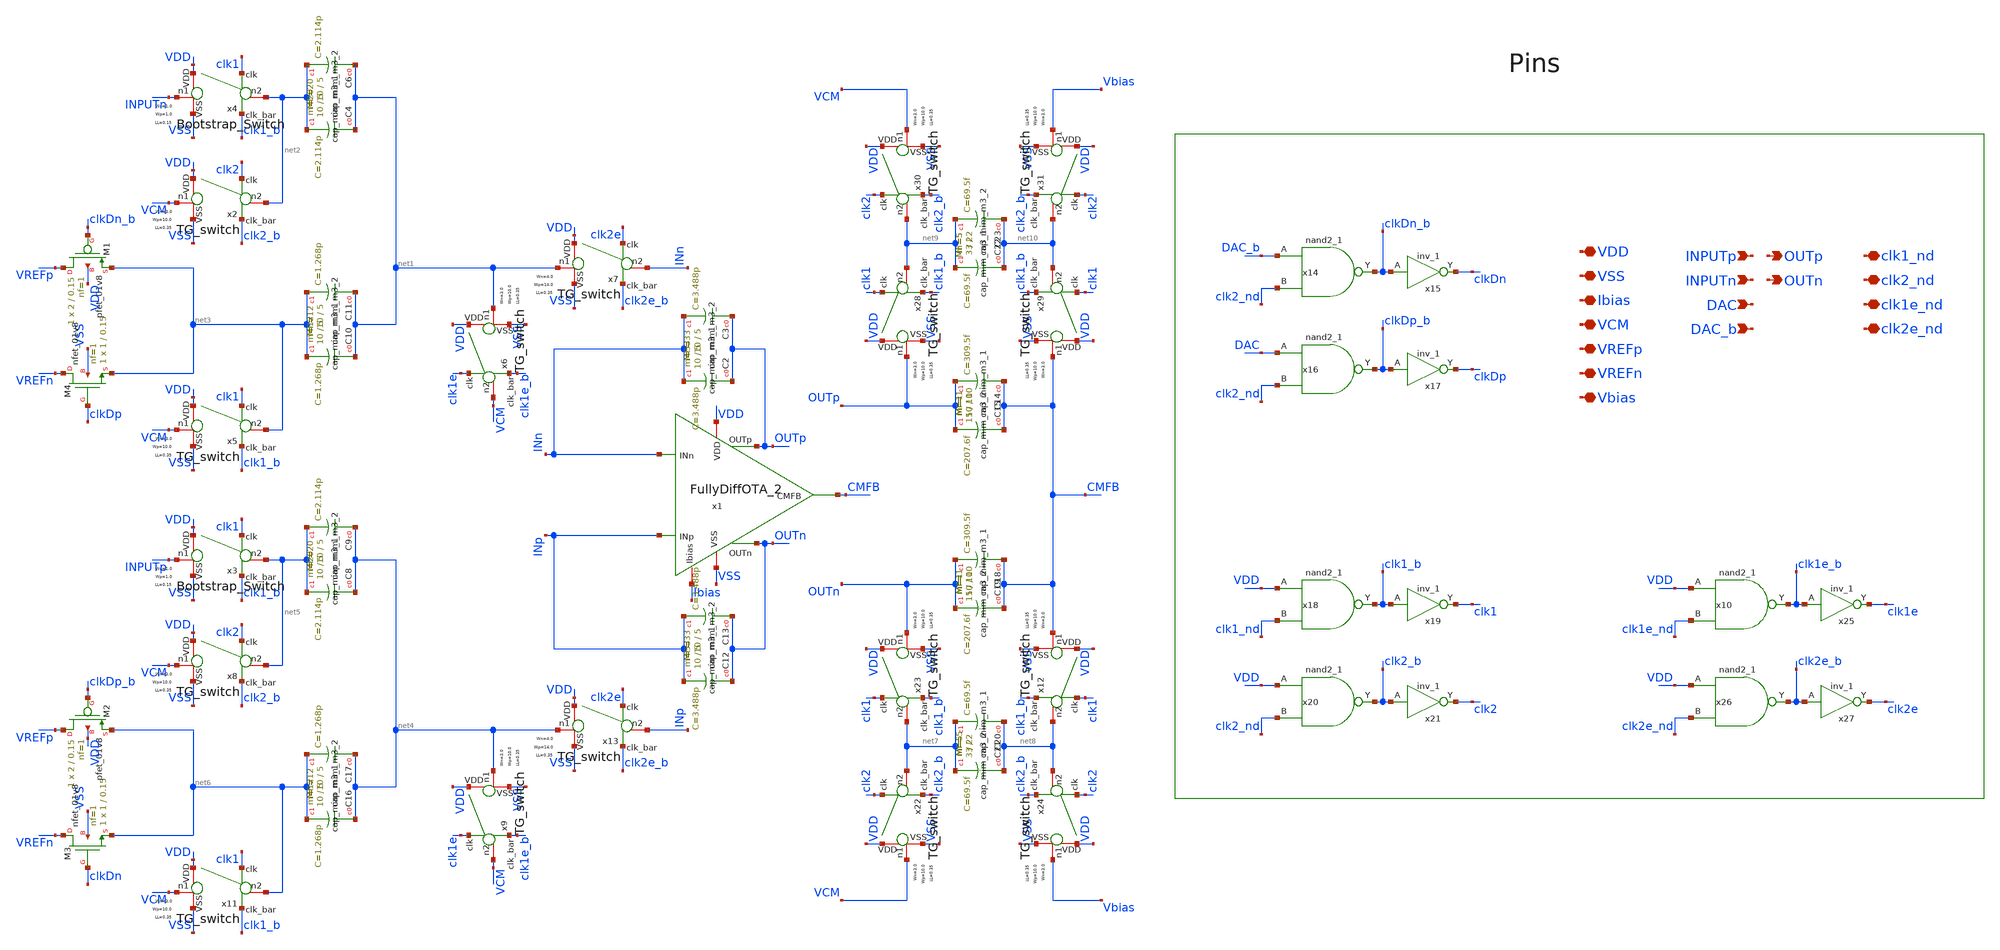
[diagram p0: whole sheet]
** sch_path: xschem/lib/Analog/SC_Integrator_2.sch
**.subckt SC_Integrator_2 clk2e_nd clk1e_nd clk2_nd clk1_nd VDD VSS VCM Ibias INPUTp INPUTn VREFp
*+ VREFn Vbias DAC DAC_b OUTp OUTn
*.iopin clk2e_nd
*.iopin clk1e_nd
*.iopin clk2_nd
*.iopin clk1_nd
*.iopin VDD
*.iopin VSS
*.iopin VCM
*.iopin Ibias
*.ipin INPUTp
*.ipin INPUTn
*.iopin VREFp
*.iopin VREFn
*.iopin Vbias
*.ipin DAC
*.ipin DAC_b
*.opin OUTp
*.opin OUTn
x14 DAC_b clk2_nd VSS VSS VDD VDD clkDn_b sky130_fd_sc_hd__nand2_1
x15 clkDn_b VSS VSS VDD VDD clkDn sky130_fd_sc_hd__inv_1
x16 DAC clk2_nd VSS VSS VDD VDD clkDp_b sky130_fd_sc_hd__nand2_1
x17 clkDp_b VSS VSS VDD VDD clkDp sky130_fd_sc_hd__inv_1
x18 VDD clk1_nd VSS VSS VDD VDD clk1_b sky130_fd_sc_hd__nand2_1
x19 clk1_b VSS VSS VDD VDD clk1 sky130_fd_sc_hd__inv_1
x20 VDD clk2_nd VSS VSS VDD VDD clk2_b sky130_fd_sc_hd__nand2_1
x21 clk2_b VSS VSS VDD VDD clk2 sky130_fd_sc_hd__inv_1
x10 VDD clk1e_nd VSS VSS VDD VDD clk1e_b sky130_fd_sc_hd__nand2_1
x25 clk1e_b VSS VSS VDD VDD clk1e sky130_fd_sc_hd__inv_1
x26 VDD clk2e_nd VSS VSS VDD VDD clk2e_b sky130_fd_sc_hd__nand2_1
x27 clk2e_b VSS VSS VDD VDD clk2e sky130_fd_sc_hd__inv_1
XM2 VREFp clkDp_b net6 VDD sky130_fd_pr__pfet_01v8 L=0.15 W=2 nf=1 ad='int((1 + 1)/2) * 2 / 1 * 0.29'
+ as='int((1 + 2)/2) * 2 / 1 * 0.29' pd='2*int((1 + 1)/2) * (2 / 1 + 0.29)' ps='2*int((1 + 2)/2) * (2 / 1 + 0.29)'
+ nrd='0.29 / 2 ' nrs='0.29 / 2 ' sa=0 sb=0 sd=0 mult=1 m=1
XM1 VREFp clkDn_b net3 VDD sky130_fd_pr__pfet_01v8 L=0.15 W=2 nf=1 ad='int((1 + 1)/2) * 2 / 1 * 0.29'
+ as='int((1 + 2)/2) * 2 / 1 * 0.29' pd='2*int((1 + 1)/2) * (2 / 1 + 0.29)' ps='2*int((1 + 2)/2) * (2 / 1 + 0.29)'
+ nrd='0.29 / 2 ' nrs='0.29 / 2 ' sa=0 sb=0 sd=0 mult=1 m=1
XM3 VREFn clkDn net6 VSS sky130_fd_pr__nfet_01v8 L=0.15 W=1 nf=1 ad='int((1 + 1)/2) * 1 / 1 * 0.29' as='int((1 + 2)/2) * 1 / 1 * 0.29'
+ pd='2*int((1 + 1)/2) * (1 / 1 + 0.29)' ps='2*int((1 + 2)/2) * (1 / 1 + 0.29)' nrd='0.29 / 1 ' nrs='0.29 / 1 '
+ sa=0 sb=0 sd=0 mult=1 m=1
XM4 VREFn clkDp net3 VSS sky130_fd_pr__nfet_01v8 L=0.15 W=1 nf=1 ad='int((1 + 1)/2) * 1 / 1 * 0.29' as='int((1 + 2)/2) * 1 / 1 * 0.29'
+ pd='2*int((1 + 1)/2) * (1 / 1 + 0.29)' ps='2*int((1 + 2)/2) * (1 / 1 + 0.29)' nrd='0.29 / 1 ' nrs='0.29 / 1 '
+ sa=0 sb=0 sd=0 mult=1 m=1
x4 clk1_b clk1 VDD VSS INPUTn net2 Bootstrap_Switch Wn=1.0 Wp=1.0 LL=0.15
x3 clk1_b clk1 VDD VSS INPUTp net5 Bootstrap_Switch Wn=1.0 Wp=1.0 LL=0.15
x6 clk1e_b clk1e VDD VSS net1 VCM TG_switch Wn=3.0 Wp=10.0 LL=0.35
x9 clk1e_b clk1e VDD VSS net4 VCM TG_switch Wn=3.0 Wp=10.0 LL=0.35
x2 clk2_b clk2 VDD VSS VCM net2 TG_switch Wn=3.0 Wp=10.0 LL=0.35
x5 clk1_b clk1 VDD VSS VCM net3 TG_switch Wn=3.0 Wp=10.0 LL=0.35
x8 clk2_b clk2 VDD VSS VCM net5 TG_switch Wn=3.0 Wp=10.0 LL=0.35
x11 clk1_b clk1 VDD VSS VCM net6 TG_switch Wn=3.0 Wp=10.0 LL=0.35
x7 clk2e_b clk2e VDD VSS net1 INn TG_switch Wn=4.0 Wp=14.0 LL=0.35
x13 clk2e_b clk2e VDD VSS net4 INp TG_switch Wn=4.0 Wp=14.0 LL=0.35
XC14 CMFB OUTp sky130_fd_pr__cap_mim_m3_2 W=15 L=10 MF=1 m=1
XC15 CMFB OUTp sky130_fd_pr__cap_mim_m3_1 W=10 L=10 MF=1 m=1
XC18 CMFB OUTn sky130_fd_pr__cap_mim_m3_2 W=15 L=10 MF=1 m=1
XC19 CMFB OUTn sky130_fd_pr__cap_mim_m3_1 W=10 L=10 MF=1 m=1
x23 clk1_b clk1 VDD VSS OUTn net7 TG_switch Wn=3.0 Wp=10.0 LL=0.35
x12 clk1_b clk1 VDD VSS CMFB net8 TG_switch Wn=3.0 Wp=10.0 LL=0.35
x22 clk2_b clk2 VDD VSS VCM net7 TG_switch Wn=3.0 Wp=10.0 LL=0.35
x24 clk2_b clk2 VDD VSS Vbias net8 TG_switch Wn=3.0 Wp=10.0 LL=0.35
XC20 net8 net7 sky130_fd_pr__cap_mim_m3_2 W=3 L=2 MF=5 m=5
XC21 net8 net7 sky130_fd_pr__cap_mim_m3_1 W=3 L=2 MF=5 m=5
x28 clk1_b clk1 VDD VSS OUTp net9 TG_switch Wn=3.0 Wp=10.0 LL=0.35
x29 clk1_b clk1 VDD VSS CMFB net10 TG_switch Wn=3.0 Wp=10.0 LL=0.35
x30 clk2_b clk2 VDD VSS VCM net9 TG_switch Wn=3.0 Wp=10.0 LL=0.35
x31 clk2_b clk2 VDD VSS Vbias net10 TG_switch Wn=3.0 Wp=10.0 LL=0.35
XC22 net10 net9 sky130_fd_pr__cap_mim_m3_2 W=3 L=2 MF=5 m=5
XC23 net10 net9 sky130_fd_pr__cap_mim_m3_1 W=3 L=2 MF=5 m=5
XC4 net1 net2 sky130_fd_pr__cap_mim_m3_2 W=10 L=5 MF=20 m=20
XC6 net1 net2 sky130_fd_pr__cap_mim_m3_1 W=10 L=5 MF=20 m=20
XC8 net4 net5 sky130_fd_pr__cap_mim_m3_2 W=10 L=5 MF=20 m=20
XC9 net4 net5 sky130_fd_pr__cap_mim_m3_1 W=10 L=5 MF=20 m=20
XC10 net1 net3 sky130_fd_pr__cap_mim_m3_2 W=10 L=5 MF=12 m=12
XC11 net1 net3 sky130_fd_pr__cap_mim_m3_1 W=10 L=5 MF=12 m=12
XC16 net4 net6 sky130_fd_pr__cap_mim_m3_2 W=10 L=5 MF=12 m=12
XC17 net4 net6 sky130_fd_pr__cap_mim_m3_1 W=10 L=5 MF=12 m=12
XC2 OUTp INn sky130_fd_pr__cap_mim_m3_2 W=10 L=5 MF=33 m=33
XC3 OUTp INn sky130_fd_pr__cap_mim_m3_1 W=10 L=5 MF=33 m=33
XC12 OUTn INp sky130_fd_pr__cap_mim_m3_2 W=10 L=5 MF=33 m=33
XC13 OUTn INp sky130_fd_pr__cap_mim_m3_1 W=10 L=5 MF=33 m=33
x1 VDD Ibias INn OUTp OUTn INp VSS CMFB FullyDiffOTA_2
**.ends

* expanding   symbol:  Analog/Bootstrap_Switch.sym # of pins=6
** sym_path: xschem/lib/Analog/Bootstrap_Switch.sym
** sch_path: xschem/lib/Analog/Bootstrap_Switch.sch
.subckt Bootstrap_Switch clk_bar clk VDD VSS n1 n2  Wn=1.0 Wp=1.0 LL=0.15
*.iopin n2
*.iopin n1
*.iopin VDD
*.iopin VSS
*.ipin clk_bar
*.ipin clk
XM1 n1 G n2 VSS sky130_fd_pr__nfet_01v8 L=LL W=WN nf=1 ad='int((1 + 1)/2) * WN / 1 * 0.29' as='int((1 + 2)/2) * WN / 1 * 0.29'
+ pd='2*int((1 + 1)/2) * (WN / 1 + 0.29)' ps='2*int((1 + 2)/2) * (WN / 1 + 0.29)' nrd='0.29 / WN ' nrs='0.29 / WN '
+ sa=0 sb=0 sd=0 mult=1 m=1
XM2 CBB G n1 VSS sky130_fd_pr__nfet_01v8 L=LL W=WN nf=1 ad='int((1 + 1)/2) * WN / 1 * 0.29' as='int((1 + 2)/2) * WN / 1 * 0.29'
+ pd='2*int((1 + 1)/2) * (WN / 1 + 0.29)' ps='2*int((1 + 2)/2) * (WN / 1 + 0.29)' nrd='0.29 / WN ' nrs='0.29 / WN '
+ sa=0 sb=0 sd=0 mult=1 m=1
XC1 CBT CBB sky130_fd_pr__cap_mim_m3_1 W=3 L=3 MF=5 m=5
XC2 CBT CBB sky130_fd_pr__cap_mim_m3_2 W=3 L=3 MF=5 m=5
XM3 CBB clk_bar VSS VSS sky130_fd_pr__nfet_01v8 L=LL W=WN nf=1 ad='int((1 + 1)/2) * WN / 1 * 0.29' as='int((1 + 2)/2) * WN / 1 * 0.29'
+ pd='2*int((1 + 1)/2) * (WN / 1 + 0.29)' ps='2*int((1 + 2)/2) * (WN / 1 + 0.29)' nrd='0.29 / WN ' nrs='0.29 / WN '
+ sa=0 sb=0 sd=0 mult=1 m=1
XM6 G VDD X VSS sky130_fd_pr__nfet_01v8 L=LL W=WN nf=1 ad='int((1 + 1)/2) * WN / 1 * 0.29' as='int((1 + 2)/2) * WN / 1 * 0.29'
+ pd='2*int((1 + 1)/2) * (WN / 1 + 0.29)' ps='2*int((1 + 2)/2) * (WN / 1 + 0.29)' nrd='0.29 / WN ' nrs='0.29 / WN '
+ sa=0 sb=0 sd=0 mult=1 m=1
XM7 VDD G CBT CBT sky130_fd_pr__pfet_01v8 L=LL W=Wp nf=1 ad='int((1 + 1)/2) * Wp / 1 * 0.29' as='int((1 + 2)/2) * Wp / 1 * 0.29'
+ pd='2*int((1 + 1)/2) * (Wp / 1 + 0.29)' ps='2*int((1 + 2)/2) * (Wp / 1 + 0.29)' nrd='0.29 / Wp ' nrs='0.29 / Wp '
+ sa=0 sb=0 sd=0 mult=1 m=1
XM8 X clk_bar VSS VSS sky130_fd_pr__nfet_01v8 L=LL W=WN nf=1 ad='int((1 + 1)/2) * WN / 1 * 0.29' as='int((1 + 2)/2) * WN / 1 * 0.29'
+ pd='2*int((1 + 1)/2) * (WN / 1 + 0.29)' ps='2*int((1 + 2)/2) * (WN / 1 + 0.29)' nrd='0.29 / WN ' nrs='0.29 / WN '
+ sa=0 sb=0 sd=0 mult=1 m=1
XM4 CBT clk_bar G CBT sky130_fd_pr__pfet_01v8 L=LL W=Wp nf=1 ad='int((1 + 1)/2) * Wp / 1 * 0.29' as='int((1 + 2)/2) * Wp / 1 * 0.29'
+ pd='2*int((1 + 1)/2) * (Wp / 1 + 0.29)' ps='2*int((1 + 2)/2) * (Wp / 1 + 0.29)' nrd='0.29 / Wp ' nrs='0.29 / Wp '
+ sa=0 sb=0 sd=0 mult=1 m=1
.ends


* expanding   symbol:  Analog/TG_switch.sym # of pins=6
** sym_path: xschem/lib/Analog/TG_switch.sym
** sch_path: xschem/lib/Analog/TG_switch.sch
.subckt TG_switch clk_bar clk VDD VSS n1 n2  Wn=3.0 Wp=10.0 LL=0.35
*.iopin n2
*.iopin n1
*.iopin VDD
*.iopin VSS
*.ipin clk_bar
*.ipin clk
XM3 n1 clk n2 VSS sky130_fd_pr__nfet_01v8_lvt L=LL W=Wn nf=1 ad='int((1 + 1)/2) * Wn / 1 * 0.29' as='int((1 + 2)/2) * Wn / 1 * 0.29'
+ pd='2*int((1 + 1)/2) * (Wn / 1 + 0.29)' ps='2*int((1 + 2)/2) * (Wn / 1 + 0.29)' nrd='0.29 / Wn ' nrs='0.29 / Wn '
+ sa=0 sb=0 sd=0 mult=1 m=1
XM4 n1 clk_bar n2 VDD sky130_fd_pr__pfet_01v8_lvt L=LL W=Wp nf=1 ad='int((1 + 1)/2) * Wp / 1 * 0.29'
+ as='int((1 + 2)/2) * Wp / 1 * 0.29' pd='2*int((1 + 1)/2) * (Wp / 1 + 0.29)' ps='2*int((1 + 2)/2) * (Wp / 1 + 0.29)'
+ nrd='0.29 / Wp ' nrs='0.29 / Wp ' sa=0 sb=0 sd=0 mult=1 m=1
.ends


* expanding   symbol:  Analog/FullyDiffOTA_2.sym # of pins=8
** sym_path: xschem/lib/Analog/FullyDiffOTA_2.sym
** sch_path: xschem/lib/Analog/FullyDiffOTA_2.sch
.subckt FullyDiffOTA_2 VDD Ibias INn OUTp OUTn INp VSS CMFB
*.iopin CMFB
*.ipin INp
*.iopin VDD
*.ipin INn
*.iopin VSS
*.opin OUTp
*.opin OUTn
*.iopin Ibias
XItail net1 Ibias VDD VDD sky130_fd_pr__pfet_01v8 L=0.7 W=2.5 nf=1 ad='int((nf+1)/2) * W/nf * 0.29' as='int((nf+2)/2) * W/nf * 0.29'
+ pd='2*int((nf+1)/2) * (W/nf + 0.29)' ps='2*int((nf+2)/2) * (W/nf + 0.29)' nrd='0.29 / W' nrs='0.29 / W'
+ sa=0 sb=0 sd=0 mult=9 m=9
XM1 OUTp1 INp net1 net1 sky130_fd_pr__pfet_01v8_lvt L=1.0 W=7.3 nf=1 ad='int((1 + 1)/2) * 7.3 / 1 * 0.29'
+ as='int((1 + 2)/2) * 7.3 / 1 * 0.29' pd='2*int((1 + 1)/2) * (7.3 / 1 + 0.29)' ps='2*int((1 + 2)/2) * (7.3 / 1 + 0.29)'
+ nrd='0.29 / 7.3 ' nrs='0.29 / 7.3 ' sa=0 sb=0 sd=0 mult=10 m=10
XM2 OUTn1 INn net1 net1 sky130_fd_pr__pfet_01v8_lvt L=1.0 W=7.3 nf=1 ad='int((1 + 1)/2) * 7.3 / 1 * 0.29'
+ as='int((1 + 2)/2) * 7.3 / 1 * 0.29' pd='2*int((1 + 1)/2) * (7.3 / 1 + 0.29)' ps='2*int((1 + 2)/2) * (7.3 / 1 + 0.29)'
+ nrd='0.29 / 7.3 ' nrs='0.29 / 7.3 ' sa=0 sb=0 sd=0 mult=10 m=10
XM3 OUTp1 VCM1 VSS VSS sky130_fd_pr__nfet_01v8 L=0.45 W=2.5 nf=1 ad='int((1 + 1)/2) * 2.5 / 1 * 0.29'
+ as='int((1 + 2)/2) * 2.5 / 1 * 0.29' pd='2*int((1 + 1)/2) * (2.5 / 1 + 0.29)' ps='2*int((1 + 2)/2) * (2.5 / 1 + 0.29)'
+ nrd='0.29 / 2.5 ' nrs='0.29 / 2.5 ' sa=0 sb=0 sd=0 mult=1 m=1
XM4 OUTn1 VCM1 VSS VSS sky130_fd_pr__nfet_01v8 L=0.45 W=2.5 nf=1 ad='int((1 + 1)/2) * 2.5 / 1 * 0.29'
+ as='int((1 + 2)/2) * 2.5 / 1 * 0.29' pd='2*int((1 + 1)/2) * (2.5 / 1 + 0.29)' ps='2*int((1 + 2)/2) * (2.5 / 1 + 0.29)'
+ nrd='0.29 / 2.5 ' nrs='0.29 / 2.5 ' sa=0 sb=0 sd=0 mult=1 m=1
XM5 OUTp OUTp1 VSS VSS sky130_fd_pr__nfet_01v8 L=0.45 W=5 nf=1 ad='int((1 + 1)/2) * 5 / 1 * 0.29' as='int((1 + 2)/2) * 5 / 1 * 0.29'
+ pd='2*int((1 + 1)/2) * (5 / 1 + 0.29)' ps='2*int((1 + 2)/2) * (5 / 1 + 0.29)' nrd='0.29 / 5 ' nrs='0.29 / 5 '
+ sa=0 sb=0 sd=0 mult=3 m=3
XM6 OUTn OUTn1 VSS VSS sky130_fd_pr__nfet_01v8 L=0.45 W=5 nf=1 ad='int((1 + 1)/2) * 5 / 1 * 0.29' as='int((1 + 2)/2) * 5 / 1 * 0.29'
+ pd='2*int((1 + 1)/2) * (5 / 1 + 0.29)' ps='2*int((1 + 2)/2) * (5 / 1 + 0.29)' nrd='0.29 / 5 ' nrs='0.29 / 5 '
+ sa=0 sb=0 sd=0 mult=3 m=3
XM7 OUTp CMFB VDD VDD sky130_fd_pr__pfet_01v8 L=0.45 W=2.5 nf=1 ad='int((1 + 1)/2) * 2.5 / 1 * 0.29'
+ as='int((1 + 2)/2) * 2.5 / 1 * 0.29' pd='2*int((1 + 1)/2) * (2.5 / 1 + 0.29)' ps='2*int((1 + 2)/2) * (2.5 / 1 + 0.29)'
+ nrd='0.29 / 2.5 ' nrs='0.29 / 2.5 ' sa=0 sb=0 sd=0 mult=9 m=9
XM8 OUTn CMFB VDD VDD sky130_fd_pr__pfet_01v8 L=0.45 W=2.5 nf=1 ad='int((1 + 1)/2) * 2.5 / 1 * 0.29'
+ as='int((1 + 2)/2) * 2.5 / 1 * 0.29' pd='2*int((1 + 1)/2) * (2.5 / 1 + 0.29)' ps='2*int((1 + 2)/2) * (2.5 / 1 + 0.29)'
+ nrd='0.29 / 2.5 ' nrs='0.29 / 2.5 ' sa=0 sb=0 sd=0 mult=9 m=9
XM9 Ibias Ibias VDD VDD sky130_fd_pr__pfet_01v8 L=0.7 W=2.5 nf=1 ad='int((nf+1)/2) * W/nf * 0.29' as='int((nf+2)/2) * W/nf * 0.29'
+ pd='2*int((nf+1)/2) * (W/nf + 0.29)' ps='2*int((nf+2)/2) * (W/nf + 0.29)' nrd='0.29 / W' nrs='0.29 / W'
+ sa=0 sb=0 sd=0 mult=9 m=9
XR9 OUTp1 VCM1 VSS sky130_fd_pr__res_xhigh_po_0p35 L=53 mult=1 m=1
XR5 VCM1 OUTn1 VSS sky130_fd_pr__res_xhigh_po_0p35 L=53 mult=1 m=1
XC5 VCM1 OUTp1 sky130_fd_pr__cap_mim_m3_1 W=2 L=3 MF=1 m=1
XC6 OUTp1 VCM1 sky130_fd_pr__cap_mim_m3_2 W=2 L=3 MF=1 m=1
XC3 OUTn1 VCM1 sky130_fd_pr__cap_mim_m3_1 W=2 L=3 MF=1 m=1
XC4 VCM1 OUTn1 sky130_fd_pr__cap_mim_m3_2 W=2 L=3 MF=1 m=1
XR1 net2 OUTp1 VSS sky130_fd_pr__res_high_po W=1 L=2 mult=1 m=1
XR2 OUTn1 net3 VSS sky130_fd_pr__res_high_po W=1 L=2 mult=1 m=1
XC1 OUTp net2 sky130_fd_pr__cap_mim_m3_1 W=12 L=12 MF=1 m=1
XC2 OUTp net2 sky130_fd_pr__cap_mim_m3_1 W=12 L=12 MF=1 m=1
XC7 net3 OUTn sky130_fd_pr__cap_mim_m3_1 W=12 L=12 MF=1 m=1
XC8 net3 OUTn sky130_fd_pr__cap_mim_m3_1 W=12 L=12 MF=1 m=1
.ends

.end
